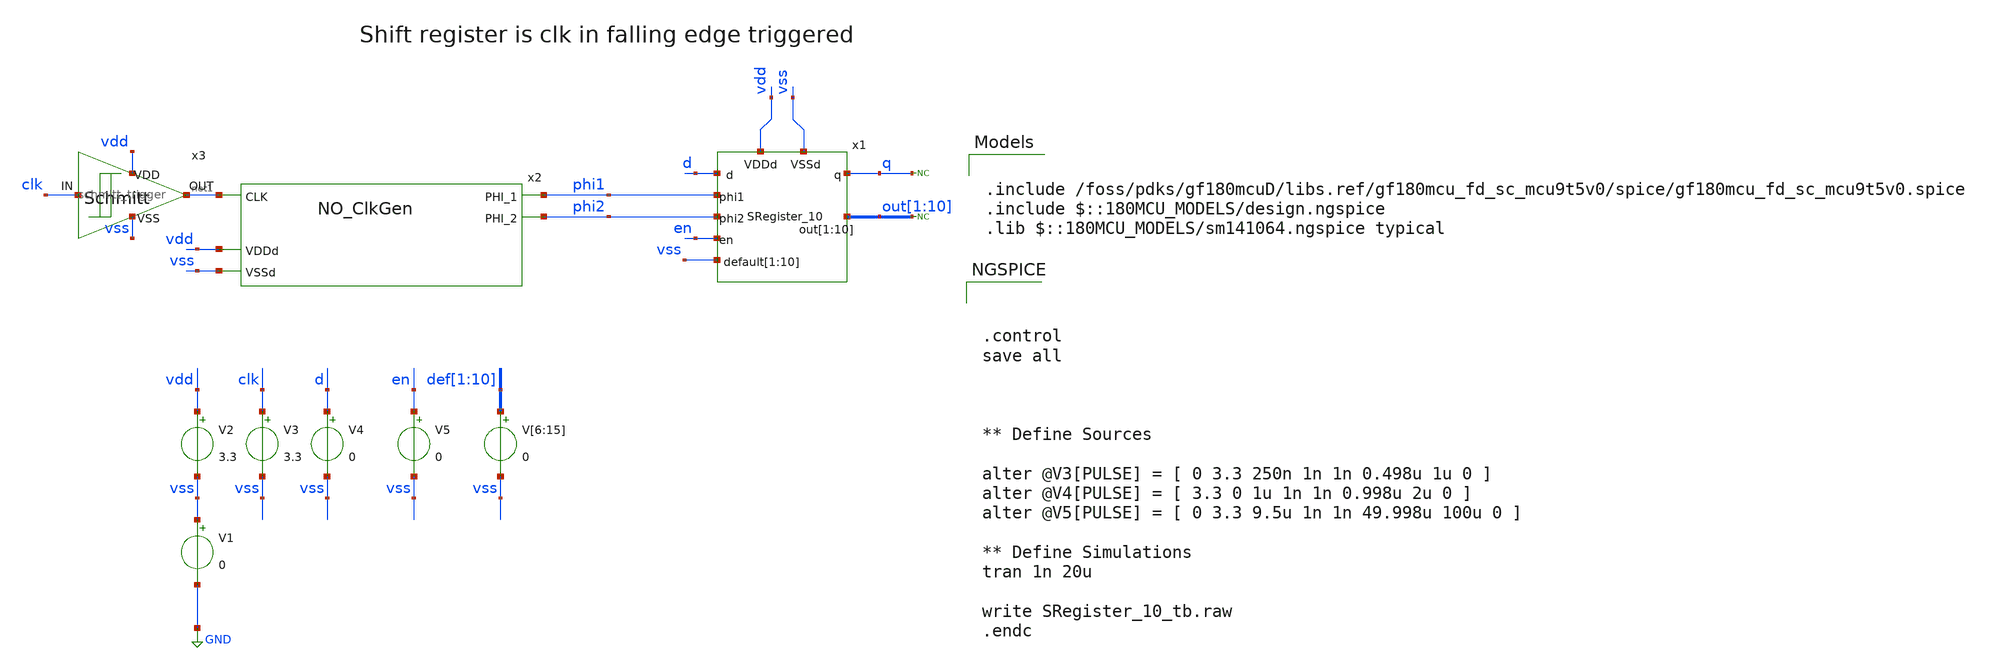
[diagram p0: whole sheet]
** sch_path: designs/libs/tb_analog/tb_SRegister_10/tb_SRegister_10.sch
**.subckt tb_SRegister_10
V1 vss GND 0
V2 vdd vss 3.3
x2 phi2 net1 phi1 vdd vss NO_ClkGen
V3 clk vss 3.3
V4 d vss 0
* noconn out[1:10]
V5 en vss 0
V[6] def[1] vss 0
V[7] def[2] vss 0
V[8] def[3] vss 0
V[9] def[4] vss 0
V[10] def[5] vss 0
V[11] def[6] vss 0
V[12] def[7] vss 0
V[13] def[8] vss 0
V[14] def[9] vss 0
V[15] def[10] vss 0
* noconn q
x1 vdd vss phi1 phi2 en vss vss vss vss vss vss vss vss vss vss d q out[1] out[2] out[3] out[4]
+ out[5] out[6] out[7] out[8] out[9] out[10] SRegister_10
x3 clk net1 vdd vss schmitt_trigger
**** begin user architecture code

.include /foss/pdks/gf180mcuD/libs.ref/gf180mcu_fd_sc_mcu9t5v0/spice/gf180mcu_fd_sc_mcu9t5v0.spice
.include $::180MCU_MODELS/design.ngspice
.lib $::180MCU_MODELS/sm141064.ngspice typical




.control
save all



** Define Sources

alter @V3[PULSE] = [ 0 3.3 250n 1n 1n 0.498u 1u 0 ]
alter @V4[PULSE] = [ 3.3 0 1u 1n 1n 0.998u 2u 0 ]
alter @V5[PULSE] = [ 0 3.3 9.5u 1n 1n 49.998u 100u 0 ]

** Define Simulations
tran 1n 20u

write SRegister_10_tb.raw
.endc


**** end user architecture code
**.ends
.GLOBAL GND
.end
